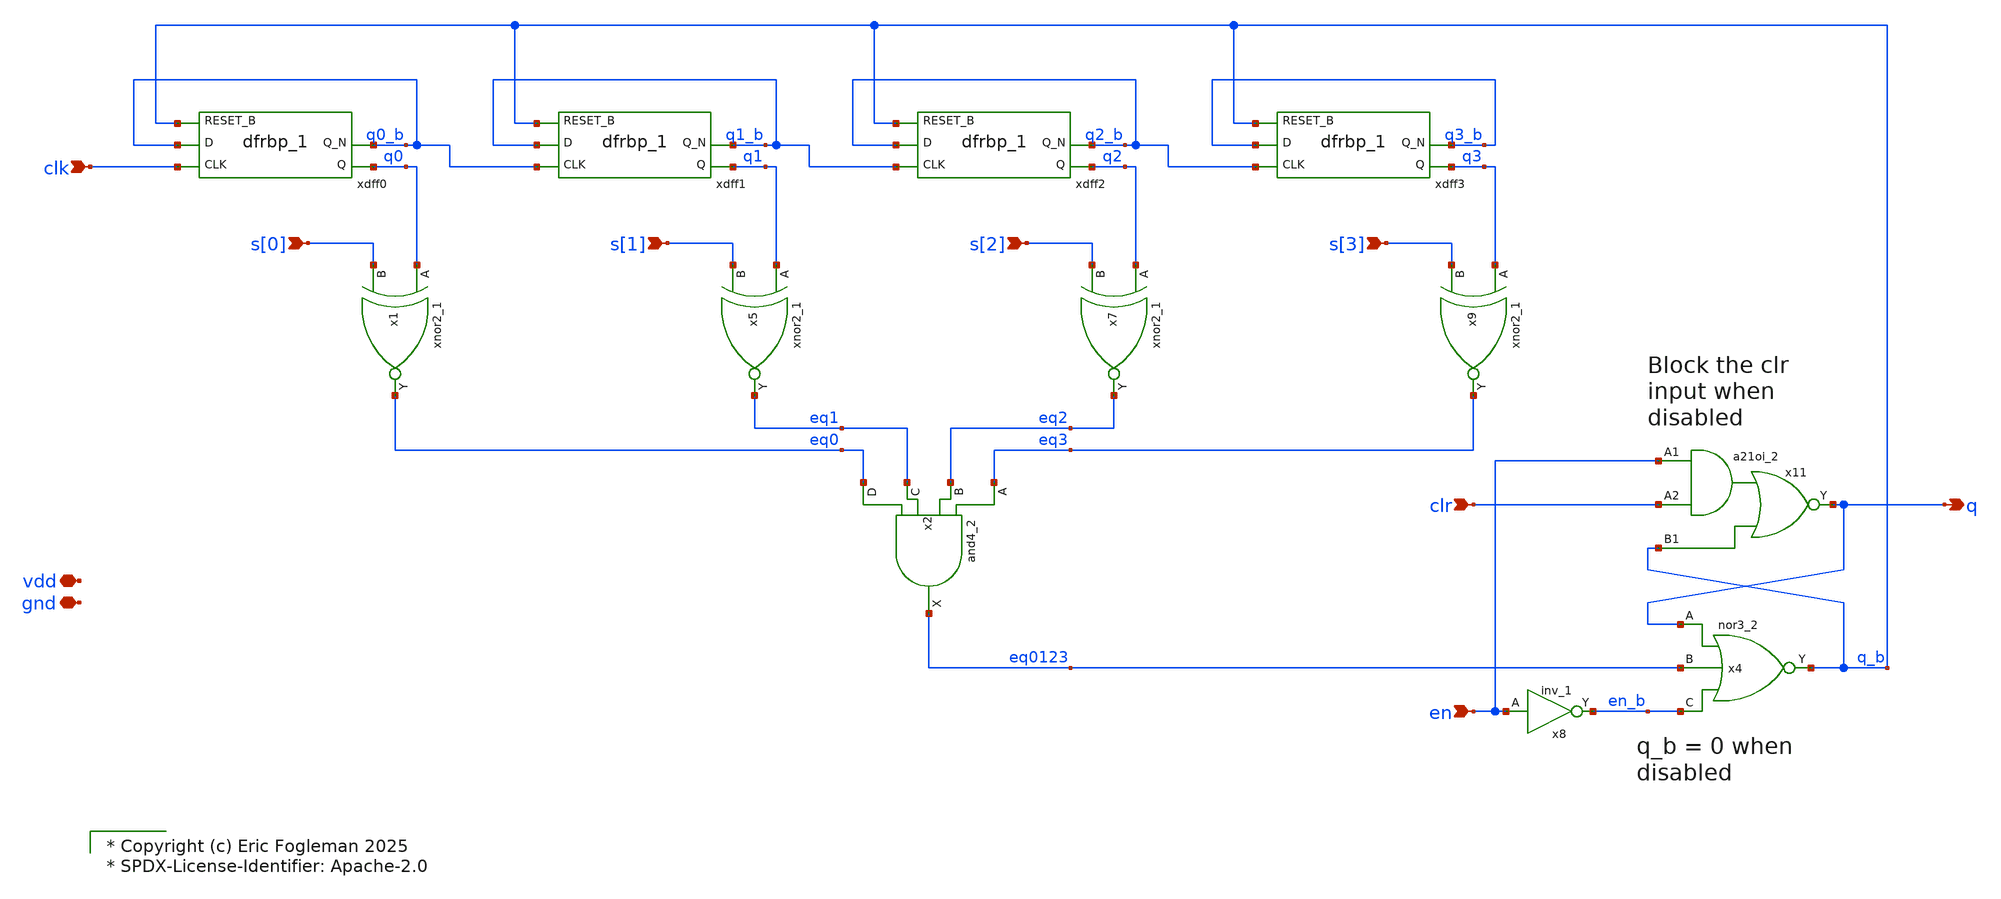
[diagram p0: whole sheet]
** sch_path: xschem/ejf_pll96_div_s.sch

* Copyright (c) Eric Fogleman 2025
* SPDX-License-Identifier: Apache-2.0

**.subckt ejf_pll96_div_s s[0] s[1] s[2] s[3] clk vdd gnd en clr q
*.ipin s[0]
*.ipin s[1]
*.ipin s[2]
*.ipin s[3]
*.ipin clk
*.iopin vdd
*.iopin gnd
*.ipin en
*.ipin clr
*.opin q
x1 q0 s[0] gnd gnd vdd vdd eq0 sky130_fd_sc_ls__xnor2_1
xdff0 clk q0_b q_b gnd gnd vdd vdd q0 q0_b sky130_fd_sc_ls__dfrbp_1
x5 q1 s[1] gnd gnd vdd vdd eq1 sky130_fd_sc_ls__xnor2_1
xdff1 q0_b q1_b q_b gnd gnd vdd vdd q1 q1_b sky130_fd_sc_ls__dfrbp_1
x7 q2 s[2] gnd gnd vdd vdd eq2 sky130_fd_sc_ls__xnor2_1
xdff2 q1_b q2_b q_b gnd gnd vdd vdd q2 q2_b sky130_fd_sc_ls__dfrbp_1
x9 q3 s[3] gnd gnd vdd vdd eq3 sky130_fd_sc_ls__xnor2_1
xdff3 q2_b q3_b q_b gnd gnd vdd vdd q3 q3_b sky130_fd_sc_ls__dfrbp_1
x8 en gnd gnd vdd vdd en_b sky130_fd_sc_ls__inv_1
x4 q eq0123 en_b gnd gnd vdd vdd q_b sky130_fd_sc_ls__nor3_2
x2 eq3 eq2 eq1 eq0 gnd gnd vdd vdd eq0123 sky130_fd_sc_ls__and4_2
x11 en clr q_b gnd gnd vdd vdd q sky130_fd_sc_ls__a21oi_2
**.ends
.end
